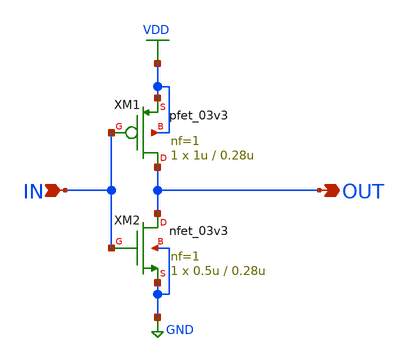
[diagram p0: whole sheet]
** sch_path: AND/INV.sch
**.subckt INV IN OUT
*.ipin IN
*.opin OUT
XM1 OUT IN VDD VDD pfet_03v3 L=0.28u W=1u nf=1 ad='int((nf+1)/2) * W/nf * 0.18u' as='int((nf+2)/2) * W/nf * 0.18u'
+ pd='2*int((nf+1)/2) * (W/nf + 0.18u)' ps='2*int((nf+2)/2) * (W/nf + 0.18u)' nrd='0.18u / W' nrs='0.18u / W'
+ sa=0 sb=0 sd=0 m=1
XM2 OUT IN GND GND nfet_03v3 L=0.28u W=0.5u nf=1 ad='int((nf+1)/2) * W/nf * 0.18u' as='int((nf+2)/2) * W/nf * 0.18u'
+ pd='2*int((nf+1)/2) * (W/nf + 0.18u)' ps='2*int((nf+2)/2) * (W/nf + 0.18u)' nrd='0.18u / W' nrs='0.18u / W'
+ sa=0 sb=0 sd=0 m=1
**.ends
.GLOBAL VDD
.GLOBAL GND
.end
